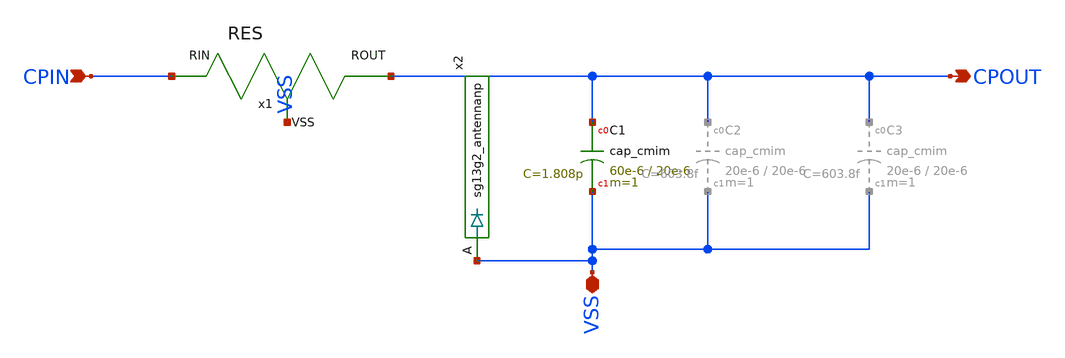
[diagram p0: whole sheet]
** sch_path: QDLL6501-main/schematic/xschem/CP.sch
* IHP-GmbH/IHP-Open-PDK/ihp-sg13g2/libs.tech/xschem/sg13g2_stdcells/sg13g2_antennanp.sch:
* Copyright 2023 IHP PDK Authors
* Licensed under the Apache License, Version 2.0 (the "License");
**.subckt CP VSS CPIN CPOUT
*.iopin VSS
*.ipin CPIN
*.opin CPOUT
XC1 CPOUT VSS cap_cmim w=60e-6 l=20e-6 m=1 mm_ok=1
x1 CPOUT CPIN VSS RES
x2 VSS CPOUT VSS sg13g2_antennanp
**.ends

* expanding   symbol:  RES.sym # of pins=3
** sym_path: QDLL6501-main/schematic/xschem/RES.sym
** sch_path: QDLL6501-main/schematic/xschem/RES.sch
.subckt RES ROUT RIN VSS
*.ipin RIN
*.opin ROUT
*.iopin VSS
XR13 net1 RIN VSS rppd w=1e-6 l=10e-6 m=1 b=0 mm_ok=1
XR1 net2 net1 VSS rppd w=1e-6 l=10e-6 m=1 b=0 mm_ok=1
XR2 net3 net2 VSS rppd w=1e-6 l=10e-6 m=1 b=0 mm_ok=1
XR3 net4 net3 VSS rppd w=1e-6 l=10e-6 m=1 b=0 mm_ok=1
XR4 net5 net4 VSS rppd w=1e-6 l=10e-6 m=1 b=0 mm_ok=1
XR5 net6 net5 VSS rppd w=1e-6 l=10e-6 m=1 b=0 mm_ok=1
XR6 net7 net6 VSS rppd w=1e-6 l=10e-6 m=1 b=0 mm_ok=1
XR7 net8 net7 VSS rppd w=1e-6 l=10e-6 m=1 b=0 mm_ok=1
XR8 net9 net8 VSS rppd w=1e-6 l=10e-6 m=1 b=0 mm_ok=1
XR9 net10 net9 VSS rppd w=1e-6 l=10e-6 m=1 b=0 mm_ok=1
XR10 net11 net10 VSS rppd w=1e-6 l=10e-6 m=1 b=0 mm_ok=1
XR11 ROUT net11 VSS rppd w=1e-6 l=10e-6 m=1 b=0 mm_ok=1
.ends


* expanding   symbol:  sg13g2_antennanp.sym # of pins=1
** sym_path: sg13g2_antennanp.sym
** sch_path: sg13g2_antennanp.sch
.subckt sg13g2_antennanp A VDD VSS
*.ipin A
*.iopin VDD
*.iopin VSS
XD1 VSS A dantenna l=0.78u w=0.78u
XD2 A VDD dpantenna l=1.34u w=1.05u
.ends

.end
